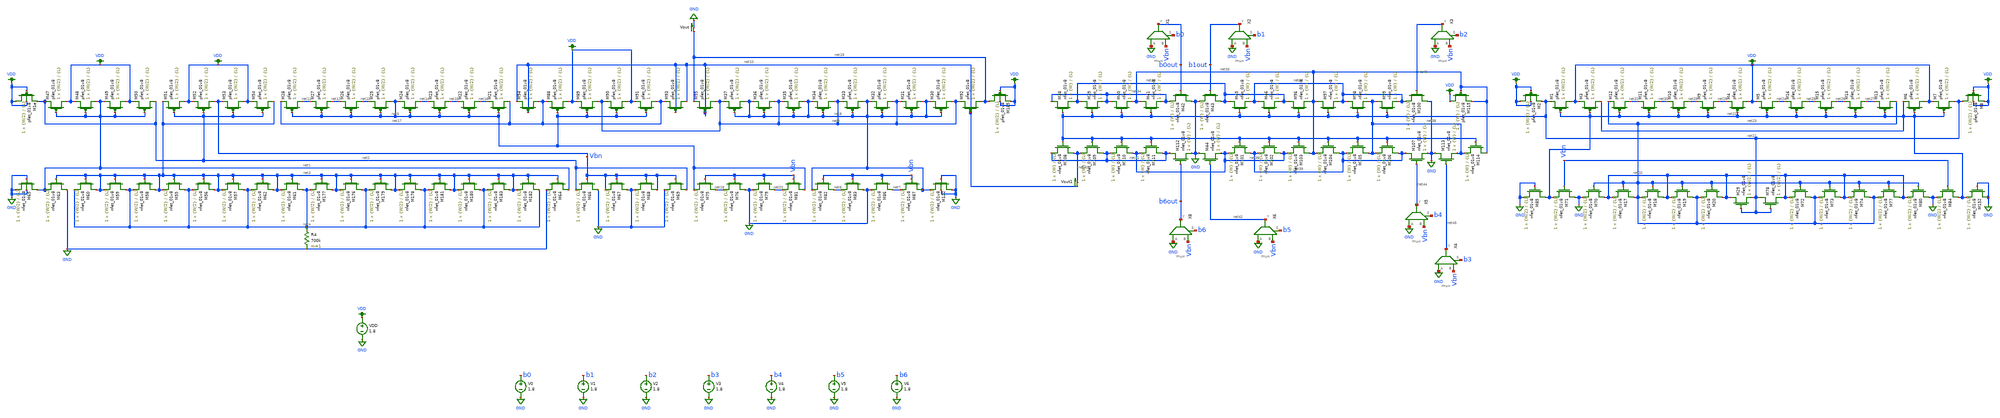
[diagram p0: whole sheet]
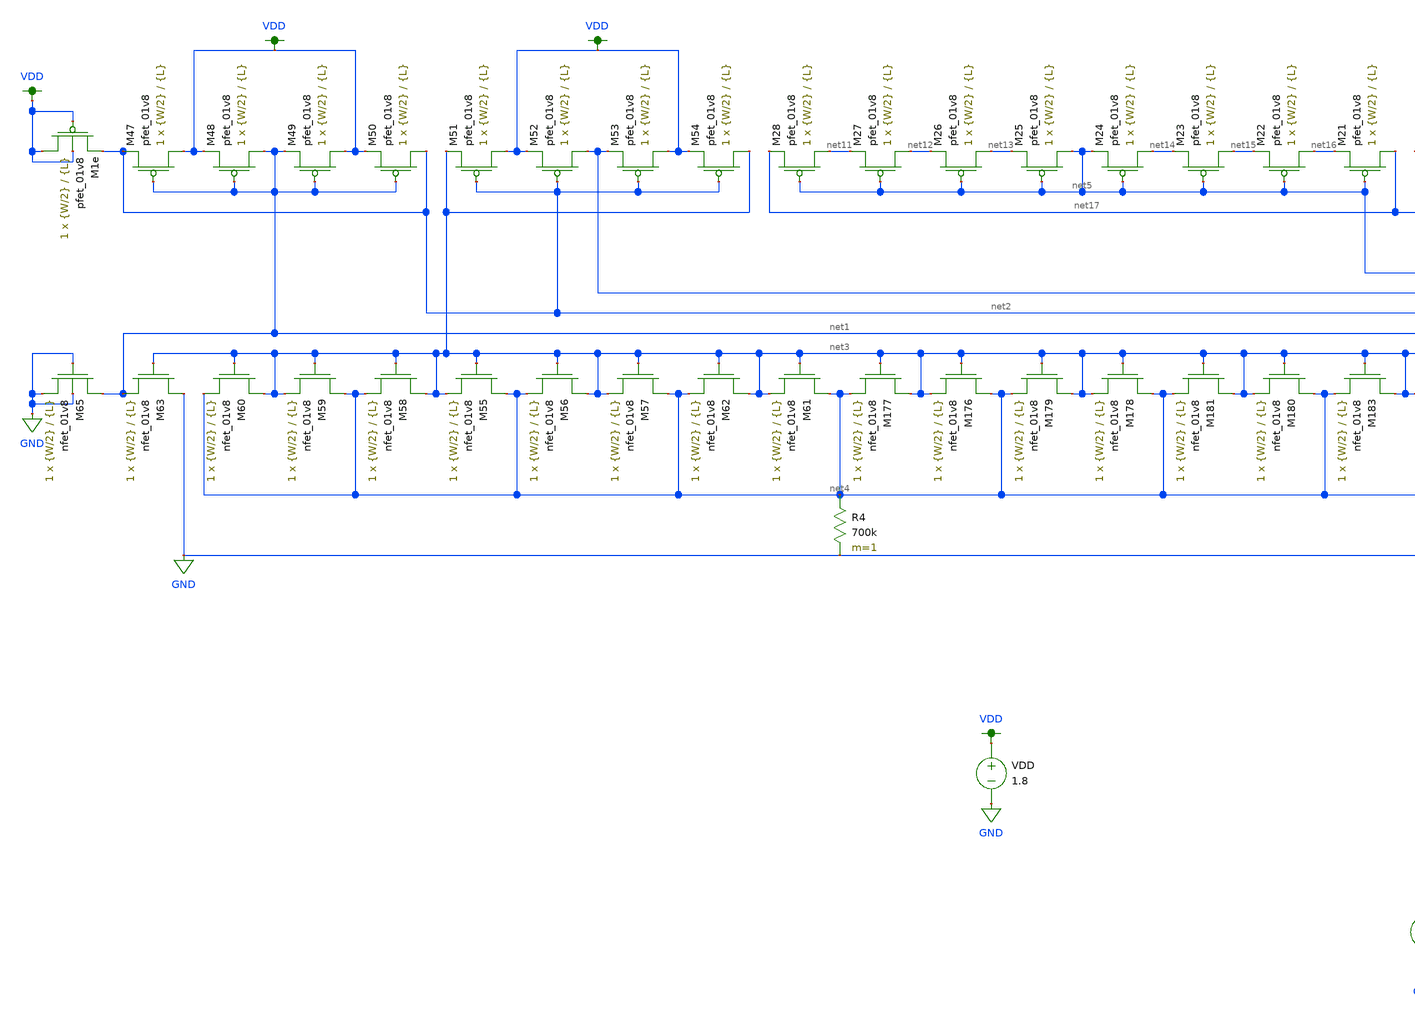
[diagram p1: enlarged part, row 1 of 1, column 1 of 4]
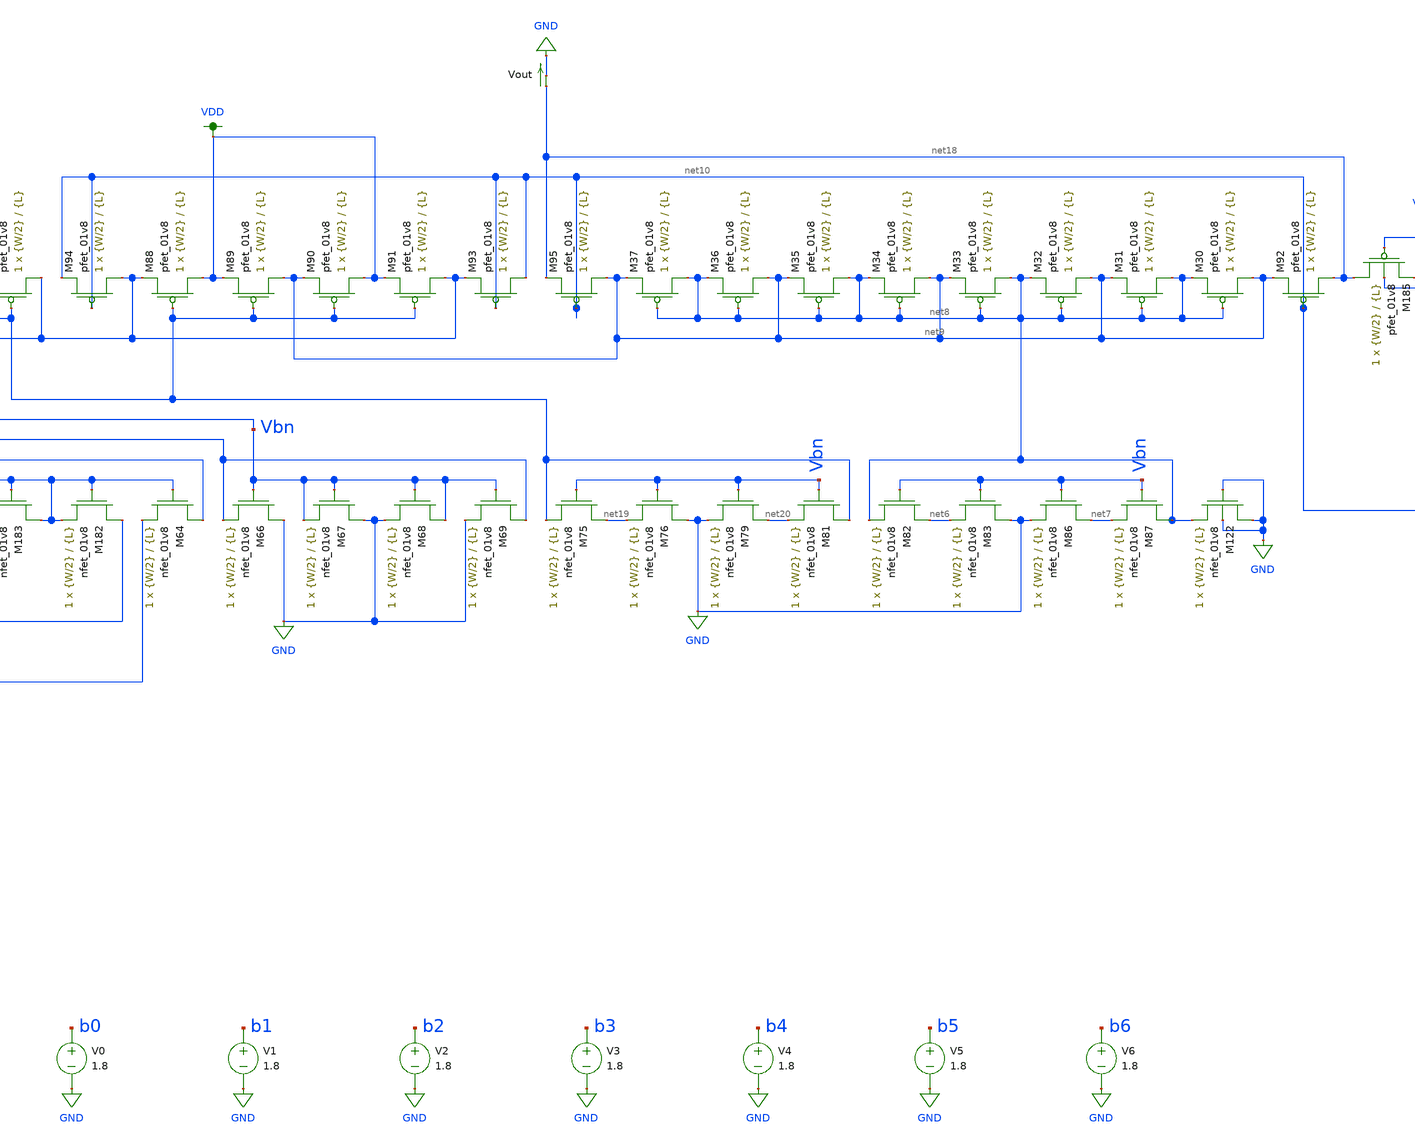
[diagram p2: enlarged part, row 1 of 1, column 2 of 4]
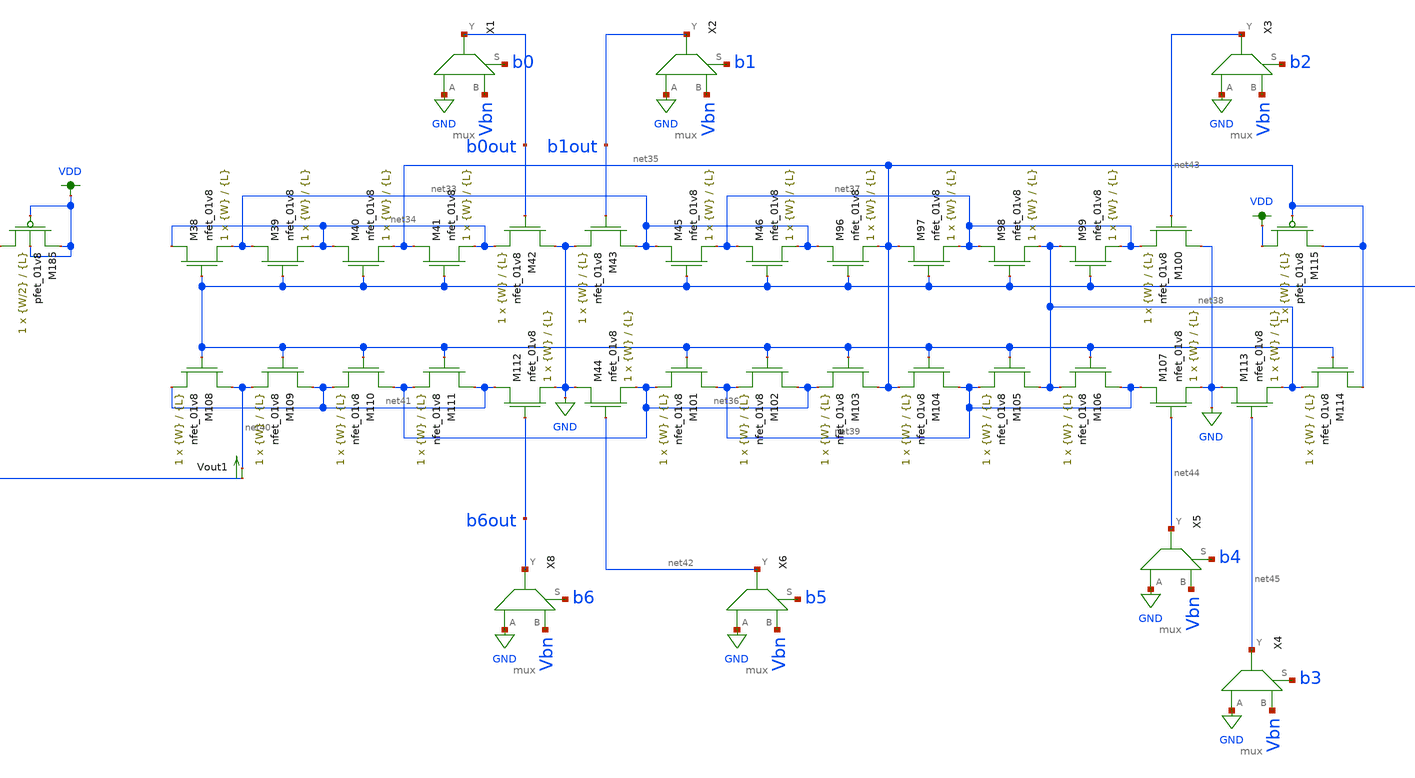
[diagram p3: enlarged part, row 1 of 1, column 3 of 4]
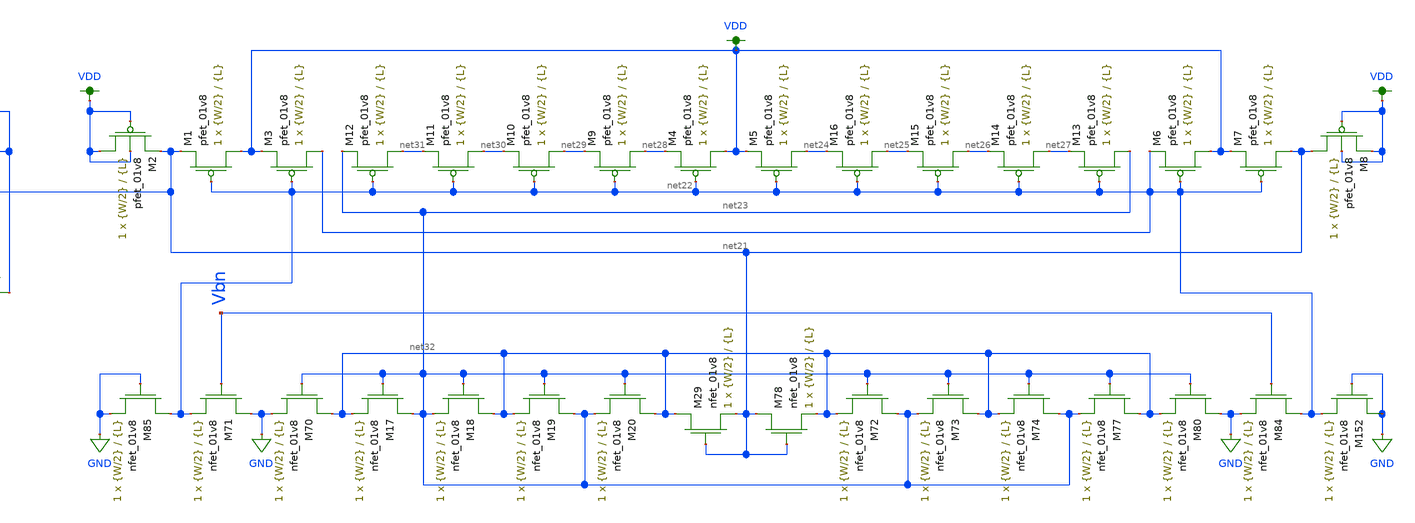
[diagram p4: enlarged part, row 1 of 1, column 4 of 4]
** sch_path: dac/schematics/misc/dac_dnl_inl_current_mirror_lds.sch
**.subckt dac_dnl_inl_current_mirror_lds
V0 b0 GND 1.8
V1 b1 GND 1.8
V2 b2 GND 1.8
V3 b3 GND 1.8
V4 b4 GND 1.8
V5 b5 GND 1.8
V6 b6 GND 1.8
VDD VDD GND 1.8
XM47 VDD net1 net2 VDD sky130_fd_pr__pfet_01v8 L={L} W={W/2} nf=1 ad='int((nf+1)/2) * W/nf * 0.29' as='int((nf+2)/2) * W/nf * 0.29'
+ pd='2*int((nf+1)/2) * (W/nf + 0.29)' ps='2*int((nf+2)/2) * (W/nf + 0.29)' nrd='0.29 / W' nrs='0.29 / W'
+ sa=0 sb=0 sd=0 mult=1 m=1
XM48 net1 net1 VDD VDD sky130_fd_pr__pfet_01v8 L={L} W={W/2} nf=1 ad='int((nf+1)/2) * W/nf * 0.29' as='int((nf+2)/2) * W/nf * 0.29'
+ pd='2*int((nf+1)/2) * (W/nf + 0.29)' ps='2*int((nf+2)/2) * (W/nf + 0.29)' nrd='0.29 / W' nrs='0.29 / W'
+ sa=0 sb=0 sd=0 mult=1 m=1
XM49 VDD net1 net1 VDD sky130_fd_pr__pfet_01v8 L={L} W={W/2} nf=1 ad='int((nf+1)/2) * W/nf * 0.29' as='int((nf+2)/2) * W/nf * 0.29'
+ pd='2*int((nf+1)/2) * (W/nf + 0.29)' ps='2*int((nf+2)/2) * (W/nf + 0.29)' nrd='0.29 / W' nrs='0.29 / W'
+ sa=0 sb=0 sd=0 mult=1 m=1
XM50 net2 net1 VDD VDD sky130_fd_pr__pfet_01v8 L={L} W={W/2} nf=1 ad='int((nf+1)/2) * W/nf * 0.29' as='int((nf+2)/2) * W/nf * 0.29'
+ pd='2*int((nf+1)/2) * (W/nf + 0.29)' ps='2*int((nf+2)/2) * (W/nf + 0.29)' nrd='0.29 / W' nrs='0.29 / W'
+ sa=0 sb=0 sd=0 mult=1 m=1
XM51 VDD net2 net3 VDD sky130_fd_pr__pfet_01v8 L={L} W={W/2} nf=1 ad='int((nf+1)/2) * W/nf * 0.29' as='int((nf+2)/2) * W/nf * 0.29'
+ pd='2*int((nf+1)/2) * (W/nf + 0.29)' ps='2*int((nf+2)/2) * (W/nf + 0.29)' nrd='0.29 / W' nrs='0.29 / W'
+ sa=0 sb=0 sd=0 mult=1 m=1
XM52 Vbn net2 VDD VDD sky130_fd_pr__pfet_01v8 L={L} W={W/2} nf=1 ad='int((nf+1)/2) * W/nf * 0.29' as='int((nf+2)/2) * W/nf * 0.29'
+ pd='2*int((nf+1)/2) * (W/nf + 0.29)' ps='2*int((nf+2)/2) * (W/nf + 0.29)' nrd='0.29 / W' nrs='0.29 / W'
+ sa=0 sb=0 sd=0 mult=1 m=1
XM53 VDD net2 Vbn VDD sky130_fd_pr__pfet_01v8 L={L} W={W/2} nf=1 ad='int((nf+1)/2) * W/nf * 0.29' as='int((nf+2)/2) * W/nf * 0.29'
+ pd='2*int((nf+1)/2) * (W/nf + 0.29)' ps='2*int((nf+2)/2) * (W/nf + 0.29)' nrd='0.29 / W' nrs='0.29 / W'
+ sa=0 sb=0 sd=0 mult=1 m=1
XM54 net3 net2 VDD VDD sky130_fd_pr__pfet_01v8 L={L} W={W/2} nf=1 ad='int((nf+1)/2) * W/nf * 0.29' as='int((nf+2)/2) * W/nf * 0.29'
+ pd='2*int((nf+1)/2) * (W/nf + 0.29)' ps='2*int((nf+2)/2) * (W/nf + 0.29)' nrd='0.29 / W' nrs='0.29 / W'
+ sa=0 sb=0 sd=0 mult=1 m=1
XM55 net4 net3 net3 GND sky130_fd_pr__nfet_01v8 L={L} W={W/2} nf=1 ad='int((nf+1)/2) * W/nf * 0.29' as='int((nf+2)/2) * W/nf * 0.29'
+ pd='2*int((nf+1)/2) * (W/nf + 0.29)' ps='2*int((nf+2)/2) * (W/nf + 0.29)' nrd='0.29 / W' nrs='0.29 / W'
+ sa=0 sb=0 sd=0 mult=1 m=1
XM56 net3 net3 net4 GND sky130_fd_pr__nfet_01v8 L={L} W={W/2} nf=1 ad='int((nf+1)/2) * W/nf * 0.29' as='int((nf+2)/2) * W/nf * 0.29'
+ pd='2*int((nf+1)/2) * (W/nf + 0.29)' ps='2*int((nf+2)/2) * (W/nf + 0.29)' nrd='0.29 / W' nrs='0.29 / W'
+ sa=0 sb=0 sd=0 mult=1 m=1
XM57 net4 net3 net3 GND sky130_fd_pr__nfet_01v8 L={L} W={W/2} nf=1 ad='int((nf+1)/2) * W/nf * 0.29' as='int((nf+2)/2) * W/nf * 0.29'
+ pd='2*int((nf+1)/2) * (W/nf + 0.29)' ps='2*int((nf+2)/2) * (W/nf + 0.29)' nrd='0.29 / W' nrs='0.29 / W'
+ sa=0 sb=0 sd=0 mult=1 m=1
XM58 net3 net3 net4 GND sky130_fd_pr__nfet_01v8 L={L} W={W/2} nf=1 ad='int((nf+1)/2) * W/nf * 0.29' as='int((nf+2)/2) * W/nf * 0.29'
+ pd='2*int((nf+1)/2) * (W/nf + 0.29)' ps='2*int((nf+2)/2) * (W/nf + 0.29)' nrd='0.29 / W' nrs='0.29 / W'
+ sa=0 sb=0 sd=0 mult=1 m=1
XM59 net4 net3 net3 GND sky130_fd_pr__nfet_01v8 L={L} W={W/2} nf=1 ad='int((nf+1)/2) * W/nf * 0.29' as='int((nf+2)/2) * W/nf * 0.29'
+ pd='2*int((nf+1)/2) * (W/nf + 0.29)' ps='2*int((nf+2)/2) * (W/nf + 0.29)' nrd='0.29 / W' nrs='0.29 / W'
+ sa=0 sb=0 sd=0 mult=1 m=1
XM60 net3 net3 net4 GND sky130_fd_pr__nfet_01v8 L={L} W={W/2} nf=1 ad='int((nf+1)/2) * W/nf * 0.29' as='int((nf+2)/2) * W/nf * 0.29'
+ pd='2*int((nf+1)/2) * (W/nf + 0.29)' ps='2*int((nf+2)/2) * (W/nf + 0.29)' nrd='0.29 / W' nrs='0.29 / W'
+ sa=0 sb=0 sd=0 mult=1 m=1
XM61 net4 net3 net3 GND sky130_fd_pr__nfet_01v8 L={L} W={W/2} nf=1 ad='int((nf+1)/2) * W/nf * 0.29' as='int((nf+2)/2) * W/nf * 0.29'
+ pd='2*int((nf+1)/2) * (W/nf + 0.29)' ps='2*int((nf+2)/2) * (W/nf + 0.29)' nrd='0.29 / W' nrs='0.29 / W'
+ sa=0 sb=0 sd=0 mult=1 m=1
XM62 net3 net3 net4 GND sky130_fd_pr__nfet_01v8 L={L} W={W/2} nf=1 ad='int((nf+1)/2) * W/nf * 0.29' as='int((nf+2)/2) * W/nf * 0.29'
+ pd='2*int((nf+1)/2) * (W/nf + 0.29)' ps='2*int((nf+2)/2) * (W/nf + 0.29)' nrd='0.29 / W' nrs='0.29 / W'
+ sa=0 sb=0 sd=0 mult=1 m=1
XM63 GND net3 net1 GND sky130_fd_pr__nfet_01v8 L={L} W={W/2} nf=1 ad='int((nf+1)/2) * W/nf * 0.29' as='int((nf+2)/2) * W/nf * 0.29'
+ pd='2*int((nf+1)/2) * (W/nf + 0.29)' ps='2*int((nf+2)/2) * (W/nf + 0.29)' nrd='0.29 / W' nrs='0.29 / W'
+ sa=0 sb=0 sd=0 mult=1 m=1
XM64 net1 net3 GND GND sky130_fd_pr__nfet_01v8 L={L} W={W/2} nf=1 ad='int((nf+1)/2) * W/nf * 0.29' as='int((nf+2)/2) * W/nf * 0.29'
+ pd='2*int((nf+1)/2) * (W/nf + 0.29)' ps='2*int((nf+2)/2) * (W/nf + 0.29)' nrd='0.29 / W' nrs='0.29 / W'
+ sa=0 sb=0 sd=0 mult=1 m=1
R4 net4 GND 700k m=1
XM1e VDD VDD net2 VDD sky130_fd_pr__pfet_01v8 L={L} W={W/2} nf=1 ad='int((nf+1)/2) * W/nf * 0.29' as='int((nf+2)/2) * W/nf * 0.29'
+ pd='2*int((nf+1)/2) * (W/nf + 0.29)' ps='2*int((nf+2)/2) * (W/nf + 0.29)' nrd='0.29 / W' nrs='0.29 / W'
+ sa=0 sb=0 sd=0 mult=1 m=1
XM65 net1 GND GND GND sky130_fd_pr__nfet_01v8 L={L} W={W/2} nf=1 ad='int((nf+1)/2) * W/nf * 0.29' as='int((nf+2)/2) * W/nf * 0.29'
+ pd='2*int((nf+1)/2) * (W/nf + 0.29)' ps='2*int((nf+2)/2) * (W/nf + 0.29)' nrd='0.29 / W' nrs='0.29 / W'
+ sa=0 sb=0 sd=0 mult=1 m=1
XM66 GND Vbn net2 GND sky130_fd_pr__nfet_01v8 L={L} W={W/2} nf=1 ad='int((nf+1)/2) * W/nf * 0.29' as='int((nf+2)/2) * W/nf * 0.29'
+ pd='2*int((nf+1)/2) * (W/nf + 0.29)' ps='2*int((nf+2)/2) * (W/nf + 0.29)' nrd='0.29 / W' nrs='0.29 / W'
+ sa=0 sb=0 sd=0 mult=1 m=1
XM67 GND Vbn Vbn GND sky130_fd_pr__nfet_01v8 L={L} W={W/2} nf=1 ad='int((nf+1)/2) * W/nf * 0.29' as='int((nf+2)/2) * W/nf * 0.29'
+ pd='2*int((nf+1)/2) * (W/nf + 0.29)' ps='2*int((nf+2)/2) * (W/nf + 0.29)' nrd='0.29 / W' nrs='0.29 / W'
+ sa=0 sb=0 sd=0 mult=1 m=1
XM68 Vbn Vbn GND GND sky130_fd_pr__nfet_01v8 L={L} W={W/2} nf=1 ad='int((nf+1)/2) * W/nf * 0.29' as='int((nf+2)/2) * W/nf * 0.29'
+ pd='2*int((nf+1)/2) * (W/nf + 0.29)' ps='2*int((nf+2)/2) * (W/nf + 0.29)' nrd='0.29 / W' nrs='0.29 / W'
+ sa=0 sb=0 sd=0 mult=1 m=1
XM69 net2 Vbn GND GND sky130_fd_pr__nfet_01v8 L={L} W={W/2} nf=1 ad='int((nf+1)/2) * W/nf * 0.29' as='int((nf+2)/2) * W/nf * 0.29'
+ pd='2*int((nf+1)/2) * (W/nf + 0.29)' ps='2*int((nf+2)/2) * (W/nf + 0.29)' nrd='0.29 / W' nrs='0.29 / W'
+ sa=0 sb=0 sd=0 mult=1 m=1
XM75 net19 Vbn net5 GND sky130_fd_pr__nfet_01v8 L={L} W={W/2} nf=1 ad='int((nf+1)/2) * W/nf * 0.29' as='int((nf+2)/2) * W/nf * 0.29'
+ pd='2*int((nf+1)/2) * (W/nf + 0.29)' ps='2*int((nf+2)/2) * (W/nf + 0.29)' nrd='0.29 / W' nrs='0.29 / W'
+ sa=0 sb=0 sd=0 mult=1 m=1
XM76 GND Vbn net19 GND sky130_fd_pr__nfet_01v8 L={L} W={W/2} nf=1 ad='int((nf+1)/2) * W/nf * 0.29' as='int((nf+2)/2) * W/nf * 0.29'
+ pd='2*int((nf+1)/2) * (W/nf + 0.29)' ps='2*int((nf+2)/2) * (W/nf + 0.29)' nrd='0.29 / W' nrs='0.29 / W'
+ sa=0 sb=0 sd=0 mult=1 m=1
XM79 net20 Vbn GND GND sky130_fd_pr__nfet_01v8 L={L} W={W/2} nf=1 ad='int((nf+1)/2) * W/nf * 0.29' as='int((nf+2)/2) * W/nf * 0.29'
+ pd='2*int((nf+1)/2) * (W/nf + 0.29)' ps='2*int((nf+2)/2) * (W/nf + 0.29)' nrd='0.29 / W' nrs='0.29 / W'
+ sa=0 sb=0 sd=0 mult=1 m=1
XM81 net5 Vbn net20 GND sky130_fd_pr__nfet_01v8 L={L} W={W/2} nf=1 ad='int((nf+1)/2) * W/nf * 0.29' as='int((nf+2)/2) * W/nf * 0.29'
+ pd='2*int((nf+1)/2) * (W/nf + 0.29)' ps='2*int((nf+2)/2) * (W/nf + 0.29)' nrd='0.29 / W' nrs='0.29 / W'
+ sa=0 sb=0 sd=0 mult=1 m=1
XM82 net6 Vbn net8 GND sky130_fd_pr__nfet_01v8 L={L} W={W/2} nf=1 ad='int((nf+1)/2) * W/nf * 0.29' as='int((nf+2)/2) * W/nf * 0.29'
+ pd='2*int((nf+1)/2) * (W/nf + 0.29)' ps='2*int((nf+2)/2) * (W/nf + 0.29)' nrd='0.29 / W' nrs='0.29 / W'
+ sa=0 sb=0 sd=0 mult=1 m=1
XM83 GND Vbn net6 GND sky130_fd_pr__nfet_01v8 L={L} W={W/2} nf=1 ad='int((nf+1)/2) * W/nf * 0.29' as='int((nf+2)/2) * W/nf * 0.29'
+ pd='2*int((nf+1)/2) * (W/nf + 0.29)' ps='2*int((nf+2)/2) * (W/nf + 0.29)' nrd='0.29 / W' nrs='0.29 / W'
+ sa=0 sb=0 sd=0 mult=1 m=1
XM86 net7 Vbn GND GND sky130_fd_pr__nfet_01v8 L={L} W={W/2} nf=1 ad='int((nf+1)/2) * W/nf * 0.29' as='int((nf+2)/2) * W/nf * 0.29'
+ pd='2*int((nf+1)/2) * (W/nf + 0.29)' ps='2*int((nf+2)/2) * (W/nf + 0.29)' nrd='0.29 / W' nrs='0.29 / W'
+ sa=0 sb=0 sd=0 mult=1 m=1
XM87 net8 Vbn net7 GND sky130_fd_pr__nfet_01v8 L={L} W={W/2} nf=1 ad='int((nf+1)/2) * W/nf * 0.29' as='int((nf+2)/2) * W/nf * 0.29'
+ pd='2*int((nf+1)/2) * (W/nf + 0.29)' ps='2*int((nf+2)/2) * (W/nf + 0.29)' nrd='0.29 / W' nrs='0.29 / W'
+ sa=0 sb=0 sd=0 mult=1 m=1
XM88 VDD net5 net17 VDD sky130_fd_pr__pfet_01v8 L={L} W={W/2} nf=1 ad='int((nf+1)/2) * W/nf * 0.29' as='int((nf+2)/2) * W/nf * 0.29'
+ pd='2*int((nf+1)/2) * (W/nf + 0.29)' ps='2*int((nf+2)/2) * (W/nf + 0.29)' nrd='0.29 / W' nrs='0.29 / W'
+ sa=0 sb=0 sd=0 mult=1 m=1
XM89 net9 net5 VDD VDD sky130_fd_pr__pfet_01v8 L={L} W={W/2} nf=1 ad='int((nf+1)/2) * W/nf * 0.29' as='int((nf+2)/2) * W/nf * 0.29'
+ pd='2*int((nf+1)/2) * (W/nf + 0.29)' ps='2*int((nf+2)/2) * (W/nf + 0.29)' nrd='0.29 / W' nrs='0.29 / W'
+ sa=0 sb=0 sd=0 mult=1 m=1
XM90 VDD net5 net9 VDD sky130_fd_pr__pfet_01v8 L={L} W={W/2} nf=1 ad='int((nf+1)/2) * W/nf * 0.29' as='int((nf+2)/2) * W/nf * 0.29'
+ pd='2*int((nf+1)/2) * (W/nf + 0.29)' ps='2*int((nf+2)/2) * (W/nf + 0.29)' nrd='0.29 / W' nrs='0.29 / W'
+ sa=0 sb=0 sd=0 mult=1 m=1
XM91 net17 net5 VDD VDD sky130_fd_pr__pfet_01v8 L={L} W={W/2} nf=1 ad='int((nf+1)/2) * W/nf * 0.29' as='int((nf+2)/2) * W/nf * 0.29'
+ pd='2*int((nf+1)/2) * (W/nf + 0.29)' ps='2*int((nf+2)/2) * (W/nf + 0.29)' nrd='0.29 / W' nrs='0.29 / W'
+ sa=0 sb=0 sd=0 mult=1 m=1
XM92 net18 net10 net9 VDD sky130_fd_pr__pfet_01v8 L={L} W={W/2} nf=1 ad='int((nf+1)/2) * W/nf * 0.29'
+ as='int((nf+2)/2) * W/nf * 0.29' pd='2*int((nf+1)/2) * (W/nf + 0.29)' ps='2*int((nf+2)/2) * (W/nf + 0.29)'
+ nrd='0.29 / W' nrs='0.29 / W' sa=0 sb=0 sd=0 mult=1 m=1
XM93 net10 net10 net17 VDD sky130_fd_pr__pfet_01v8 L={L} W={W/2} nf=1 ad='int((nf+1)/2) * W/nf * 0.29'
+ as='int((nf+2)/2) * W/nf * 0.29' pd='2*int((nf+1)/2) * (W/nf + 0.29)' ps='2*int((nf+2)/2) * (W/nf + 0.29)'
+ nrd='0.29 / W' nrs='0.29 / W' sa=0 sb=0 sd=0 mult=1 m=1
XM94 net17 net10 net10 VDD sky130_fd_pr__pfet_01v8 L={L} W={W/2} nf=1 ad='int((nf+1)/2) * W/nf * 0.29'
+ as='int((nf+2)/2) * W/nf * 0.29' pd='2*int((nf+1)/2) * (W/nf + 0.29)' ps='2*int((nf+2)/2) * (W/nf + 0.29)'
+ nrd='0.29 / W' nrs='0.29 / W' sa=0 sb=0 sd=0 mult=1 m=1
XM95 net9 net10 net18 VDD sky130_fd_pr__pfet_01v8 L={L} W={W/2} nf=1 ad='int((nf+1)/2) * W/nf * 0.29'
+ as='int((nf+2)/2) * W/nf * 0.29' pd='2*int((nf+1)/2) * (W/nf + 0.29)' ps='2*int((nf+2)/2) * (W/nf + 0.29)'
+ nrd='0.29 / W' nrs='0.29 / W' sa=0 sb=0 sd=0 mult=1 m=1
XM176 net4 net3 net3 GND sky130_fd_pr__nfet_01v8 L={L} W={W/2} nf=1 ad='int((nf+1)/2) * W/nf * 0.29'
+ as='int((nf+2)/2) * W/nf * 0.29' pd='2*int((nf+1)/2) * (W/nf + 0.29)' ps='2*int((nf+2)/2) * (W/nf + 0.29)'
+ nrd='0.29 / W' nrs='0.29 / W' sa=0 sb=0 sd=0 mult=1 m=1
XM177 net3 net3 net4 GND sky130_fd_pr__nfet_01v8 L={L} W={W/2} nf=1 ad='int((nf+1)/2) * W/nf * 0.29'
+ as='int((nf+2)/2) * W/nf * 0.29' pd='2*int((nf+1)/2) * (W/nf + 0.29)' ps='2*int((nf+2)/2) * (W/nf + 0.29)'
+ nrd='0.29 / W' nrs='0.29 / W' sa=0 sb=0 sd=0 mult=1 m=1
XM178 net4 net3 net3 GND sky130_fd_pr__nfet_01v8 L={L} W={W/2} nf=1 ad='int((nf+1)/2) * W/nf * 0.29'
+ as='int((nf+2)/2) * W/nf * 0.29' pd='2*int((nf+1)/2) * (W/nf + 0.29)' ps='2*int((nf+2)/2) * (W/nf + 0.29)'
+ nrd='0.29 / W' nrs='0.29 / W' sa=0 sb=0 sd=0 mult=1 m=1
XM179 net3 net3 net4 GND sky130_fd_pr__nfet_01v8 L={L} W={W/2} nf=1 ad='int((nf+1)/2) * W/nf * 0.29'
+ as='int((nf+2)/2) * W/nf * 0.29' pd='2*int((nf+1)/2) * (W/nf + 0.29)' ps='2*int((nf+2)/2) * (W/nf + 0.29)'
+ nrd='0.29 / W' nrs='0.29 / W' sa=0 sb=0 sd=0 mult=1 m=1
XM180 net4 net3 net3 GND sky130_fd_pr__nfet_01v8 L={L} W={W/2} nf=1 ad='int((nf+1)/2) * W/nf * 0.29'
+ as='int((nf+2)/2) * W/nf * 0.29' pd='2*int((nf+1)/2) * (W/nf + 0.29)' ps='2*int((nf+2)/2) * (W/nf + 0.29)'
+ nrd='0.29 / W' nrs='0.29 / W' sa=0 sb=0 sd=0 mult=1 m=1
XM181 net3 net3 net4 GND sky130_fd_pr__nfet_01v8 L={L} W={W/2} nf=1 ad='int((nf+1)/2) * W/nf * 0.29'
+ as='int((nf+2)/2) * W/nf * 0.29' pd='2*int((nf+1)/2) * (W/nf + 0.29)' ps='2*int((nf+2)/2) * (W/nf + 0.29)'
+ nrd='0.29 / W' nrs='0.29 / W' sa=0 sb=0 sd=0 mult=1 m=1
XM182 net4 net3 net3 GND sky130_fd_pr__nfet_01v8 L={L} W={W/2} nf=1 ad='int((nf+1)/2) * W/nf * 0.29'
+ as='int((nf+2)/2) * W/nf * 0.29' pd='2*int((nf+1)/2) * (W/nf + 0.29)' ps='2*int((nf+2)/2) * (W/nf + 0.29)'
+ nrd='0.29 / W' nrs='0.29 / W' sa=0 sb=0 sd=0 mult=1 m=1
XM183 net3 net3 net4 GND sky130_fd_pr__nfet_01v8 L={L} W={W/2} nf=1 ad='int((nf+1)/2) * W/nf * 0.29'
+ as='int((nf+2)/2) * W/nf * 0.29' pd='2*int((nf+1)/2) * (W/nf + 0.29)' ps='2*int((nf+2)/2) * (W/nf + 0.29)'
+ nrd='0.29 / W' nrs='0.29 / W' sa=0 sb=0 sd=0 mult=1 m=1
XM185 net18 VDD VDD VDD sky130_fd_pr__pfet_01v8 L={L} W={W/2} nf=1 ad='int((nf+1)/2) * W/nf * 0.29' as='int((nf+2)/2) * W/nf * 0.29'
+ pd='2*int((nf+1)/2) * (W/nf + 0.29)' ps='2*int((nf+2)/2) * (W/nf + 0.29)' nrd='0.29 / W' nrs='0.29 / W'
+ sa=0 sb=0 sd=0 mult=1 m=1
Vout net18 GND 0
.save i(vout)
XM21 net17 net5 net16 VDD sky130_fd_pr__pfet_01v8 L={L} W={W/2} nf=1 ad='int((nf+1)/2) * W/nf * 0.29'
+ as='int((nf+2)/2) * W/nf * 0.29' pd='2*int((nf+1)/2) * (W/nf + 0.29)' ps='2*int((nf+2)/2) * (W/nf + 0.29)'
+ nrd='0.29 / W' nrs='0.29 / W' sa=0 sb=0 sd=0 mult=1 m=1
XM22 net16 net5 net15 VDD sky130_fd_pr__pfet_01v8 L={L} W={W/2} nf=1 ad='int((nf+1)/2) * W/nf * 0.29'
+ as='int((nf+2)/2) * W/nf * 0.29' pd='2*int((nf+1)/2) * (W/nf + 0.29)' ps='2*int((nf+2)/2) * (W/nf + 0.29)'
+ nrd='0.29 / W' nrs='0.29 / W' sa=0 sb=0 sd=0 mult=1 m=1
XM23 net15 net5 net14 VDD sky130_fd_pr__pfet_01v8 L={L} W={W/2} nf=1 ad='int((nf+1)/2) * W/nf * 0.29'
+ as='int((nf+2)/2) * W/nf * 0.29' pd='2*int((nf+1)/2) * (W/nf + 0.29)' ps='2*int((nf+2)/2) * (W/nf + 0.29)'
+ nrd='0.29 / W' nrs='0.29 / W' sa=0 sb=0 sd=0 mult=1 m=1
XM24 net14 net5 net5 VDD sky130_fd_pr__pfet_01v8 L={L} W={W/2} nf=1 ad='int((nf+1)/2) * W/nf * 0.29'
+ as='int((nf+2)/2) * W/nf * 0.29' pd='2*int((nf+1)/2) * (W/nf + 0.29)' ps='2*int((nf+2)/2) * (W/nf + 0.29)'
+ nrd='0.29 / W' nrs='0.29 / W' sa=0 sb=0 sd=0 mult=1 m=1
XM25 net5 net5 net13 VDD sky130_fd_pr__pfet_01v8 L={L} W={W/2} nf=1 ad='int((nf+1)/2) * W/nf * 0.29'
+ as='int((nf+2)/2) * W/nf * 0.29' pd='2*int((nf+1)/2) * (W/nf + 0.29)' ps='2*int((nf+2)/2) * (W/nf + 0.29)'
+ nrd='0.29 / W' nrs='0.29 / W' sa=0 sb=0 sd=0 mult=1 m=1
XM26 net13 net5 net12 VDD sky130_fd_pr__pfet_01v8 L={L} W={W/2} nf=1 ad='int((nf+1)/2) * W/nf * 0.29'
+ as='int((nf+2)/2) * W/nf * 0.29' pd='2*int((nf+1)/2) * (W/nf + 0.29)' ps='2*int((nf+2)/2) * (W/nf + 0.29)'
+ nrd='0.29 / W' nrs='0.29 / W' sa=0 sb=0 sd=0 mult=1 m=1
XM27 net12 net5 net11 VDD sky130_fd_pr__pfet_01v8 L={L} W={W/2} nf=1 ad='int((nf+1)/2) * W/nf * 0.29'
+ as='int((nf+2)/2) * W/nf * 0.29' pd='2*int((nf+1)/2) * (W/nf + 0.29)' ps='2*int((nf+2)/2) * (W/nf + 0.29)'
+ nrd='0.29 / W' nrs='0.29 / W' sa=0 sb=0 sd=0 mult=1 m=1
XM28 net11 net5 net17 VDD sky130_fd_pr__pfet_01v8 L={L} W={W/2} nf=1 ad='int((nf+1)/2) * W/nf * 0.29'
+ as='int((nf+2)/2) * W/nf * 0.29' pd='2*int((nf+1)/2) * (W/nf + 0.29)' ps='2*int((nf+2)/2) * (W/nf + 0.29)'
+ nrd='0.29 / W' nrs='0.29 / W' sa=0 sb=0 sd=0 mult=1 m=1
XM30 net9 net8 net8 VDD sky130_fd_pr__pfet_01v8 L={L} W={W/2} nf=1 ad='int((nf+1)/2) * W/nf * 0.29' as='int((nf+2)/2) * W/nf * 0.29'
+ pd='2*int((nf+1)/2) * (W/nf + 0.29)' ps='2*int((nf+2)/2) * (W/nf + 0.29)' nrd='0.29 / W' nrs='0.29 / W'
+ sa=0 sb=0 sd=0 mult=1 m=1
XM31 net8 net8 net9 VDD sky130_fd_pr__pfet_01v8 L={L} W={W/2} nf=1 ad='int((nf+1)/2) * W/nf * 0.29' as='int((nf+2)/2) * W/nf * 0.29'
+ pd='2*int((nf+1)/2) * (W/nf + 0.29)' ps='2*int((nf+2)/2) * (W/nf + 0.29)' nrd='0.29 / W' nrs='0.29 / W'
+ sa=0 sb=0 sd=0 mult=1 m=1
XM32 net9 net8 net8 VDD sky130_fd_pr__pfet_01v8 L={L} W={W/2} nf=1 ad='int((nf+1)/2) * W/nf * 0.29' as='int((nf+2)/2) * W/nf * 0.29'
+ pd='2*int((nf+1)/2) * (W/nf + 0.29)' ps='2*int((nf+2)/2) * (W/nf + 0.29)' nrd='0.29 / W' nrs='0.29 / W'
+ sa=0 sb=0 sd=0 mult=1 m=1
XM33 net8 net8 net9 VDD sky130_fd_pr__pfet_01v8 L={L} W={W/2} nf=1 ad='int((nf+1)/2) * W/nf * 0.29' as='int((nf+2)/2) * W/nf * 0.29'
+ pd='2*int((nf+1)/2) * (W/nf + 0.29)' ps='2*int((nf+2)/2) * (W/nf + 0.29)' nrd='0.29 / W' nrs='0.29 / W'
+ sa=0 sb=0 sd=0 mult=1 m=1
XM34 net9 net8 net8 VDD sky130_fd_pr__pfet_01v8 L={L} W={W/2} nf=1 ad='int((nf+1)/2) * W/nf * 0.29' as='int((nf+2)/2) * W/nf * 0.29'
+ pd='2*int((nf+1)/2) * (W/nf + 0.29)' ps='2*int((nf+2)/2) * (W/nf + 0.29)' nrd='0.29 / W' nrs='0.29 / W'
+ sa=0 sb=0 sd=0 mult=1 m=1
XM35 net8 net8 net9 VDD sky130_fd_pr__pfet_01v8 L={L} W={W/2} nf=1 ad='int((nf+1)/2) * W/nf * 0.29' as='int((nf+2)/2) * W/nf * 0.29'
+ pd='2*int((nf+1)/2) * (W/nf + 0.29)' ps='2*int((nf+2)/2) * (W/nf + 0.29)' nrd='0.29 / W' nrs='0.29 / W'
+ sa=0 sb=0 sd=0 mult=1 m=1
XM36 net9 net8 net8 VDD sky130_fd_pr__pfet_01v8 L={L} W={W/2} nf=1 ad='int((nf+1)/2) * W/nf * 0.29' as='int((nf+2)/2) * W/nf * 0.29'
+ pd='2*int((nf+1)/2) * (W/nf + 0.29)' ps='2*int((nf+2)/2) * (W/nf + 0.29)' nrd='0.29 / W' nrs='0.29 / W'
+ sa=0 sb=0 sd=0 mult=1 m=1
XM37 net8 net8 net9 VDD sky130_fd_pr__pfet_01v8 L={L} W={W/2} nf=1 ad='int((nf+1)/2) * W/nf * 0.29' as='int((nf+2)/2) * W/nf * 0.29'
+ pd='2*int((nf+1)/2) * (W/nf + 0.29)' ps='2*int((nf+2)/2) * (W/nf + 0.29)' nrd='0.29 / W' nrs='0.29 / W'
+ sa=0 sb=0 sd=0 mult=1 m=1
XM122 GND GND net8 GND sky130_fd_pr__nfet_01v8 L={L} W={W/2} nf=1 ad='int((nf+1)/2) * W/nf * 0.29' as='int((nf+2)/2) * W/nf * 0.29'
+ pd='2*int((nf+1)/2) * (W/nf + 0.29)' ps='2*int((nf+2)/2) * (W/nf + 0.29)' nrd='0.29 / W' nrs='0.29 / W'
+ sa=0 sb=0 sd=0 mult=1 m=1
XM1 VDD net22 net21 VDD sky130_fd_pr__pfet_01v8 L={L} W={W/2} nf=1 ad='int((nf+1)/2) * W/nf * 0.29' as='int((nf+2)/2) * W/nf * 0.29'
+ pd='2*int((nf+1)/2) * (W/nf + 0.29)' ps='2*int((nf+2)/2) * (W/nf + 0.29)' nrd='0.29 / W' nrs='0.29 / W'
+ sa=0 sb=0 sd=0 mult=1 m=1
XM2 VDD VDD net21 VDD sky130_fd_pr__pfet_01v8 L={L} W={W/2} nf=1 ad='int((nf+1)/2) * W/nf * 0.29' as='int((nf+2)/2) * W/nf * 0.29'
+ pd='2*int((nf+1)/2) * (W/nf + 0.29)' ps='2*int((nf+2)/2) * (W/nf + 0.29)' nrd='0.29 / W' nrs='0.29 / W'
+ sa=0 sb=0 sd=0 mult=1 m=1
XM3 net22 net22 VDD VDD sky130_fd_pr__pfet_01v8 L={L} W={W/2} nf=1 ad='int((nf+1)/2) * W/nf * 0.29' as='int((nf+2)/2) * W/nf * 0.29'
+ pd='2*int((nf+1)/2) * (W/nf + 0.29)' ps='2*int((nf+2)/2) * (W/nf + 0.29)' nrd='0.29 / W' nrs='0.29 / W'
+ sa=0 sb=0 sd=0 mult=1 m=1
XM4 VDD net22 net28 VDD sky130_fd_pr__pfet_01v8 L={L} W={W/2} nf=1 ad='int((nf+1)/2) * W/nf * 0.29' as='int((nf+2)/2) * W/nf * 0.29'
+ pd='2*int((nf+1)/2) * (W/nf + 0.29)' ps='2*int((nf+2)/2) * (W/nf + 0.29)' nrd='0.29 / W' nrs='0.29 / W'
+ sa=0 sb=0 sd=0 mult=1 m=1
XM5 net24 net22 VDD VDD sky130_fd_pr__pfet_01v8 L={L} W={W/2} nf=1 ad='int((nf+1)/2) * W/nf * 0.29' as='int((nf+2)/2) * W/nf * 0.29'
+ pd='2*int((nf+1)/2) * (W/nf + 0.29)' ps='2*int((nf+2)/2) * (W/nf + 0.29)' nrd='0.29 / W' nrs='0.29 / W'
+ sa=0 sb=0 sd=0 mult=1 m=1
XM6 VDD net22 net22 VDD sky130_fd_pr__pfet_01v8 L={L} W={W/2} nf=1 ad='int((nf+1)/2) * W/nf * 0.29' as='int((nf+2)/2) * W/nf * 0.29'
+ pd='2*int((nf+1)/2) * (W/nf + 0.29)' ps='2*int((nf+2)/2) * (W/nf + 0.29)' nrd='0.29 / W' nrs='0.29 / W'
+ sa=0 sb=0 sd=0 mult=1 m=1
XM7 net21 net22 VDD VDD sky130_fd_pr__pfet_01v8 L={L} W={W/2} nf=1 ad='int((nf+1)/2) * W/nf * 0.29' as='int((nf+2)/2) * W/nf * 0.29'
+ pd='2*int((nf+1)/2) * (W/nf + 0.29)' ps='2*int((nf+2)/2) * (W/nf + 0.29)' nrd='0.29 / W' nrs='0.29 / W'
+ sa=0 sb=0 sd=0 mult=1 m=1
XM8 net21 VDD VDD VDD sky130_fd_pr__pfet_01v8 L={L} W={W/2} nf=1 ad='int((nf+1)/2) * W/nf * 0.29' as='int((nf+2)/2) * W/nf * 0.29'
+ pd='2*int((nf+1)/2) * (W/nf + 0.29)' ps='2*int((nf+2)/2) * (W/nf + 0.29)' nrd='0.29 / W' nrs='0.29 / W'
+ sa=0 sb=0 sd=0 mult=1 m=1
XM9 net28 net22 net29 VDD sky130_fd_pr__pfet_01v8 L={L} W={W/2} nf=1 ad='int((nf+1)/2) * W/nf * 0.29'
+ as='int((nf+2)/2) * W/nf * 0.29' pd='2*int((nf+1)/2) * (W/nf + 0.29)' ps='2*int((nf+2)/2) * (W/nf + 0.29)'
+ nrd='0.29 / W' nrs='0.29 / W' sa=0 sb=0 sd=0 mult=1 m=1
XM10 net29 net22 net30 VDD sky130_fd_pr__pfet_01v8 L={L} W={W/2} nf=1 ad='int((nf+1)/2) * W/nf * 0.29'
+ as='int((nf+2)/2) * W/nf * 0.29' pd='2*int((nf+1)/2) * (W/nf + 0.29)' ps='2*int((nf+2)/2) * (W/nf + 0.29)'
+ nrd='0.29 / W' nrs='0.29 / W' sa=0 sb=0 sd=0 mult=1 m=1
XM11 net30 net22 net31 VDD sky130_fd_pr__pfet_01v8 L={L} W={W/2} nf=1 ad='int((nf+1)/2) * W/nf * 0.29'
+ as='int((nf+2)/2) * W/nf * 0.29' pd='2*int((nf+1)/2) * (W/nf + 0.29)' ps='2*int((nf+2)/2) * (W/nf + 0.29)'
+ nrd='0.29 / W' nrs='0.29 / W' sa=0 sb=0 sd=0 mult=1 m=1
XM12 net31 net22 net23 VDD sky130_fd_pr__pfet_01v8 L={L} W={W/2} nf=1 ad='int((nf+1)/2) * W/nf * 0.29'
+ as='int((nf+2)/2) * W/nf * 0.29' pd='2*int((nf+1)/2) * (W/nf + 0.29)' ps='2*int((nf+2)/2) * (W/nf + 0.29)'
+ nrd='0.29 / W' nrs='0.29 / W' sa=0 sb=0 sd=0 mult=1 m=1
XM13 net23 net22 net27 VDD sky130_fd_pr__pfet_01v8 L={L} W={W/2} nf=1 ad='int((nf+1)/2) * W/nf * 0.29'
+ as='int((nf+2)/2) * W/nf * 0.29' pd='2*int((nf+1)/2) * (W/nf + 0.29)' ps='2*int((nf+2)/2) * (W/nf + 0.29)'
+ nrd='0.29 / W' nrs='0.29 / W' sa=0 sb=0 sd=0 mult=1 m=1
XM14 net27 net22 net26 VDD sky130_fd_pr__pfet_01v8 L={L} W={W/2} nf=1 ad='int((nf+1)/2) * W/nf * 0.29'
+ as='int((nf+2)/2) * W/nf * 0.29' pd='2*int((nf+1)/2) * (W/nf + 0.29)' ps='2*int((nf+2)/2) * (W/nf + 0.29)'
+ nrd='0.29 / W' nrs='0.29 / W' sa=0 sb=0 sd=0 mult=1 m=1
XM15 net26 net22 net25 VDD sky130_fd_pr__pfet_01v8 L={L} W={W/2} nf=1 ad='int((nf+1)/2) * W/nf * 0.29'
+ as='int((nf+2)/2) * W/nf * 0.29' pd='2*int((nf+1)/2) * (W/nf + 0.29)' ps='2*int((nf+2)/2) * (W/nf + 0.29)'
+ nrd='0.29 / W' nrs='0.29 / W' sa=0 sb=0 sd=0 mult=1 m=1
XM16 net25 net22 net24 VDD sky130_fd_pr__pfet_01v8 L={L} W={W/2} nf=1 ad='int((nf+1)/2) * W/nf * 0.29'
+ as='int((nf+2)/2) * W/nf * 0.29' pd='2*int((nf+1)/2) * (W/nf + 0.29)' ps='2*int((nf+2)/2) * (W/nf + 0.29)'
+ nrd='0.29 / W' nrs='0.29 / W' sa=0 sb=0 sd=0 mult=1 m=1
XM17 net23 net23 net32 GND sky130_fd_pr__nfet_01v8 L={L} W={W/2} nf=1 ad='int((nf+1)/2) * W/nf * 0.29'
+ as='int((nf+2)/2) * W/nf * 0.29' pd='2*int((nf+1)/2) * (W/nf + 0.29)' ps='2*int((nf+2)/2) * (W/nf + 0.29)'
+ nrd='0.29 / W' nrs='0.29 / W' sa=0 sb=0 sd=0 mult=1 m=1
XM18 net32 net23 net23 GND sky130_fd_pr__nfet_01v8 L={L} W={W/2} nf=1 ad='int((nf+1)/2) * W/nf * 0.29'
+ as='int((nf+2)/2) * W/nf * 0.29' pd='2*int((nf+1)/2) * (W/nf + 0.29)' ps='2*int((nf+2)/2) * (W/nf + 0.29)'
+ nrd='0.29 / W' nrs='0.29 / W' sa=0 sb=0 sd=0 mult=1 m=1
XM19 net23 net23 net32 GND sky130_fd_pr__nfet_01v8 L={L} W={W/2} nf=1 ad='int((nf+1)/2) * W/nf * 0.29'
+ as='int((nf+2)/2) * W/nf * 0.29' pd='2*int((nf+1)/2) * (W/nf + 0.29)' ps='2*int((nf+2)/2) * (W/nf + 0.29)'
+ nrd='0.29 / W' nrs='0.29 / W' sa=0 sb=0 sd=0 mult=1 m=1
XM20 net32 net23 net23 GND sky130_fd_pr__nfet_01v8 L={L} W={W/2} nf=1 ad='int((nf+1)/2) * W/nf * 0.29'
+ as='int((nf+2)/2) * W/nf * 0.29' pd='2*int((nf+1)/2) * (W/nf + 0.29)' ps='2*int((nf+2)/2) * (W/nf + 0.29)'
+ nrd='0.29 / W' nrs='0.29 / W' sa=0 sb=0 sd=0 mult=1 m=1
XM29 net32 net21 net21 GND sky130_fd_pr__nfet_01v8 L={L} W={W/2} nf=1 ad='int((nf+1)/2) * W/nf * 0.29'
+ as='int((nf+2)/2) * W/nf * 0.29' pd='2*int((nf+1)/2) * (W/nf + 0.29)' ps='2*int((nf+2)/2) * (W/nf + 0.29)'
+ nrd='0.29 / W' nrs='0.29 / W' sa=0 sb=0 sd=0 mult=1 m=1
XM70 net32 net23 GND GND sky130_fd_pr__nfet_01v8 L={L} W={W/2} nf=1 ad='int((nf+1)/2) * W/nf * 0.29'
+ as='int((nf+2)/2) * W/nf * 0.29' pd='2*int((nf+1)/2) * (W/nf + 0.29)' ps='2*int((nf+2)/2) * (W/nf + 0.29)'
+ nrd='0.29 / W' nrs='0.29 / W' sa=0 sb=0 sd=0 mult=1 m=1
XM71 GND Vbn net22 GND sky130_fd_pr__nfet_01v8 L={L} W={W/2} nf=1 ad='int((nf+1)/2) * W/nf * 0.29' as='int((nf+2)/2) * W/nf * 0.29'
+ pd='2*int((nf+1)/2) * (W/nf + 0.29)' ps='2*int((nf+2)/2) * (W/nf + 0.29)' nrd='0.29 / W' nrs='0.29 / W'
+ sa=0 sb=0 sd=0 mult=1 m=1
XM72 net23 net23 net32 GND sky130_fd_pr__nfet_01v8 L={L} W={W/2} nf=1 ad='int((nf+1)/2) * W/nf * 0.29'
+ as='int((nf+2)/2) * W/nf * 0.29' pd='2*int((nf+1)/2) * (W/nf + 0.29)' ps='2*int((nf+2)/2) * (W/nf + 0.29)'
+ nrd='0.29 / W' nrs='0.29 / W' sa=0 sb=0 sd=0 mult=1 m=1
XM73 net32 net23 net23 GND sky130_fd_pr__nfet_01v8 L={L} W={W/2} nf=1 ad='int((nf+1)/2) * W/nf * 0.29'
+ as='int((nf+2)/2) * W/nf * 0.29' pd='2*int((nf+1)/2) * (W/nf + 0.29)' ps='2*int((nf+2)/2) * (W/nf + 0.29)'
+ nrd='0.29 / W' nrs='0.29 / W' sa=0 sb=0 sd=0 mult=1 m=1
XM74 net23 net23 net32 GND sky130_fd_pr__nfet_01v8 L={L} W={W/2} nf=1 ad='int((nf+1)/2) * W/nf * 0.29'
+ as='int((nf+2)/2) * W/nf * 0.29' pd='2*int((nf+1)/2) * (W/nf + 0.29)' ps='2*int((nf+2)/2) * (W/nf + 0.29)'
+ nrd='0.29 / W' nrs='0.29 / W' sa=0 sb=0 sd=0 mult=1 m=1
XM77 net32 net23 net23 GND sky130_fd_pr__nfet_01v8 L={L} W={W/2} nf=1 ad='int((nf+1)/2) * W/nf * 0.29'
+ as='int((nf+2)/2) * W/nf * 0.29' pd='2*int((nf+1)/2) * (W/nf + 0.29)' ps='2*int((nf+2)/2) * (W/nf + 0.29)'
+ nrd='0.29 / W' nrs='0.29 / W' sa=0 sb=0 sd=0 mult=1 m=1
XM78 net21 net21 net32 GND sky130_fd_pr__nfet_01v8 L={L} W={W/2} nf=1 ad='int((nf+1)/2) * W/nf * 0.29'
+ as='int((nf+2)/2) * W/nf * 0.29' pd='2*int((nf+1)/2) * (W/nf + 0.29)' ps='2*int((nf+2)/2) * (W/nf + 0.29)'
+ nrd='0.29 / W' nrs='0.29 / W' sa=0 sb=0 sd=0 mult=1 m=1
XM80 GND net23 net32 GND sky130_fd_pr__nfet_01v8 L={L} W={W/2} nf=1 ad='int((nf+1)/2) * W/nf * 0.29'
+ as='int((nf+2)/2) * W/nf * 0.29' pd='2*int((nf+1)/2) * (W/nf + 0.29)' ps='2*int((nf+2)/2) * (W/nf + 0.29)'
+ nrd='0.29 / W' nrs='0.29 / W' sa=0 sb=0 sd=0 mult=1 m=1
XM84 net22 Vbn GND GND sky130_fd_pr__nfet_01v8 L={L} W={W/2} nf=1 ad='int((nf+1)/2) * W/nf * 0.29' as='int((nf+2)/2) * W/nf * 0.29'
+ pd='2*int((nf+1)/2) * (W/nf + 0.29)' ps='2*int((nf+2)/2) * (W/nf + 0.29)' nrd='0.29 / W' nrs='0.29 / W'
+ sa=0 sb=0 sd=0 mult=1 m=1
XM85 net22 GND GND GND sky130_fd_pr__nfet_01v8 L={L} W={W/2} nf=1 ad='int((nf+1)/2) * W/nf * 0.29' as='int((nf+2)/2) * W/nf * 0.29'
+ pd='2*int((nf+1)/2) * (W/nf + 0.29)' ps='2*int((nf+2)/2) * (W/nf + 0.29)' nrd='0.29 / W' nrs='0.29 / W'
+ sa=0 sb=0 sd=0 mult=1 m=1
XM152 GND GND net22 GND sky130_fd_pr__nfet_01v8 L={L} W={W/2} nf=1 ad='int((nf+1)/2) * W/nf * 0.29' as='int((nf+2)/2) * W/nf * 0.29'
+ pd='2*int((nf+1)/2) * (W/nf + 0.29)' ps='2*int((nf+2)/2) * (W/nf + 0.29)' nrd='0.29 / W' nrs='0.29 / W'
+ sa=0 sb=0 sd=0 mult=1 m=1
X1 GND Vbn b0out b0 mux
X2 GND Vbn b1out b1 mux
X3 GND Vbn net43 b2 mux
X4 GND Vbn net45 b3 mux
X5 GND Vbn net44 b4 mux
X6 GND Vbn net42 b5 mux
X8 GND Vbn b6out b6 mux
Vout1 net10 net40 0
.save i(vout1)
XM38 net34 net21 net33 GND sky130_fd_pr__nfet_01v8 L={L} W={W} nf=1 ad='int((nf+1)/2) * W/nf * 0.29'
+ as='int((nf+2)/2) * W/nf * 0.29' pd='2*int((nf+1)/2) * (W/nf + 0.29)' ps='2*int((nf+2)/2) * (W/nf + 0.29)'
+ nrd='0.29 / W' nrs='0.29 / W' sa=0 sb=0 sd=0 mult=1 m=1
XM39 net33 net21 net34 GND sky130_fd_pr__nfet_01v8 L={L} W={W} nf=1 ad='int((nf+1)/2) * W/nf * 0.29'
+ as='int((nf+2)/2) * W/nf * 0.29' pd='2*int((nf+1)/2) * (W/nf + 0.29)' ps='2*int((nf+2)/2) * (W/nf + 0.29)'
+ nrd='0.29 / W' nrs='0.29 / W' sa=0 sb=0 sd=0 mult=1 m=1
XM40 net34 net21 net35 GND sky130_fd_pr__nfet_01v8 L={L} W={W} nf=1 ad='int((nf+1)/2) * W/nf * 0.29'
+ as='int((nf+2)/2) * W/nf * 0.29' pd='2*int((nf+1)/2) * (W/nf + 0.29)' ps='2*int((nf+2)/2) * (W/nf + 0.29)'
+ nrd='0.29 / W' nrs='0.29 / W' sa=0 sb=0 sd=0 mult=1 m=1
XM41 net35 net21 net34 GND sky130_fd_pr__nfet_01v8 L={L} W={W} nf=1 ad='int((nf+1)/2) * W/nf * 0.29'
+ as='int((nf+2)/2) * W/nf * 0.29' pd='2*int((nf+1)/2) * (W/nf + 0.29)' ps='2*int((nf+2)/2) * (W/nf + 0.29)'
+ nrd='0.29 / W' nrs='0.29 / W' sa=0 sb=0 sd=0 mult=1 m=1
XM42 GND b0out net34 GND sky130_fd_pr__nfet_01v8 L={L} W={W} nf=1 ad='int((nf+1)/2) * W/nf * 0.29' as='int((nf+2)/2) * W/nf * 0.29'
+ pd='2*int((nf+1)/2) * (W/nf + 0.29)' ps='2*int((nf+2)/2) * (W/nf + 0.29)' nrd='0.29 / W' nrs='0.29 / W'
+ sa=0 sb=0 sd=0 mult=1 m=1
XM43 net33 b1out GND GND sky130_fd_pr__nfet_01v8 L={L} W={W} nf=1 ad='int((nf+1)/2) * W/nf * 0.29' as='int((nf+2)/2) * W/nf * 0.29'
+ pd='2*int((nf+1)/2) * (W/nf + 0.29)' ps='2*int((nf+2)/2) * (W/nf + 0.29)' nrd='0.29 / W' nrs='0.29 / W'
+ sa=0 sb=0 sd=0 mult=1 m=1
XM44 GND net42 net36 GND sky130_fd_pr__nfet_01v8 L={L} W={W} nf=1 ad='int((nf+1)/2) * W/nf * 0.29' as='int((nf+2)/2) * W/nf * 0.29'
+ pd='2*int((nf+1)/2) * (W/nf + 0.29)' ps='2*int((nf+2)/2) * (W/nf + 0.29)' nrd='0.29 / W' nrs='0.29 / W'
+ sa=0 sb=0 sd=0 mult=1 m=1
XM45 net33 net21 net37 GND sky130_fd_pr__nfet_01v8 L={L} W={W} nf=1 ad='int((nf+1)/2) * W/nf * 0.29'
+ as='int((nf+2)/2) * W/nf * 0.29' pd='2*int((nf+1)/2) * (W/nf + 0.29)' ps='2*int((nf+2)/2) * (W/nf + 0.29)'
+ nrd='0.29 / W' nrs='0.29 / W' sa=0 sb=0 sd=0 mult=1 m=1
XM46 net37 net21 net33 GND sky130_fd_pr__nfet_01v8 L={L} W={W} nf=1 ad='int((nf+1)/2) * W/nf * 0.29'
+ as='int((nf+2)/2) * W/nf * 0.29' pd='2*int((nf+1)/2) * (W/nf + 0.29)' ps='2*int((nf+2)/2) * (W/nf + 0.29)'
+ nrd='0.29 / W' nrs='0.29 / W' sa=0 sb=0 sd=0 mult=1 m=1
XM96 net33 net21 net35 GND sky130_fd_pr__nfet_01v8 L={L} W={W} nf=1 ad='int((nf+1)/2) * W/nf * 0.29'
+ as='int((nf+2)/2) * W/nf * 0.29' pd='2*int((nf+1)/2) * (W/nf + 0.29)' ps='2*int((nf+2)/2) * (W/nf + 0.29)'
+ nrd='0.29 / W' nrs='0.29 / W' sa=0 sb=0 sd=0 mult=1 m=1
XM97 net35 net21 net37 GND sky130_fd_pr__nfet_01v8 L={L} W={W} nf=1 ad='int((nf+1)/2) * W/nf * 0.29'
+ as='int((nf+2)/2) * W/nf * 0.29' pd='2*int((nf+1)/2) * (W/nf + 0.29)' ps='2*int((nf+2)/2) * (W/nf + 0.29)'
+ nrd='0.29 / W' nrs='0.29 / W' sa=0 sb=0 sd=0 mult=1 m=1
XM98 net37 net21 net38 GND sky130_fd_pr__nfet_01v8 L={L} W={W} nf=1 ad='int((nf+1)/2) * W/nf * 0.29'
+ as='int((nf+2)/2) * W/nf * 0.29' pd='2*int((nf+1)/2) * (W/nf + 0.29)' ps='2*int((nf+2)/2) * (W/nf + 0.29)'
+ nrd='0.29 / W' nrs='0.29 / W' sa=0 sb=0 sd=0 mult=1 m=1
XM99 net38 net21 net37 GND sky130_fd_pr__nfet_01v8 L={L} W={W} nf=1 ad='int((nf+1)/2) * W/nf * 0.29'
+ as='int((nf+2)/2) * W/nf * 0.29' pd='2*int((nf+1)/2) * (W/nf + 0.29)' ps='2*int((nf+2)/2) * (W/nf + 0.29)'
+ nrd='0.29 / W' nrs='0.29 / W' sa=0 sb=0 sd=0 mult=1 m=1
XM100 GND net43 net37 GND sky130_fd_pr__nfet_01v8 L={L} W={W} nf=1 ad='int((nf+1)/2) * W/nf * 0.29' as='int((nf+2)/2) * W/nf * 0.29'
+ pd='2*int((nf+1)/2) * (W/nf + 0.29)' ps='2*int((nf+2)/2) * (W/nf + 0.29)' nrd='0.29 / W' nrs='0.29 / W'
+ sa=0 sb=0 sd=0 mult=1 m=1
XM101 net39 net21 net36 GND sky130_fd_pr__nfet_01v8 L={L} W={W} nf=1 ad='int((nf+1)/2) * W/nf * 0.29'
+ as='int((nf+2)/2) * W/nf * 0.29' pd='2*int((nf+1)/2) * (W/nf + 0.29)' ps='2*int((nf+2)/2) * (W/nf + 0.29)'
+ nrd='0.29 / W' nrs='0.29 / W' sa=0 sb=0 sd=0 mult=1 m=1
XM102 net36 net21 net39 GND sky130_fd_pr__nfet_01v8 L={L} W={W} nf=1 ad='int((nf+1)/2) * W/nf * 0.29'
+ as='int((nf+2)/2) * W/nf * 0.29' pd='2*int((nf+1)/2) * (W/nf + 0.29)' ps='2*int((nf+2)/2) * (W/nf + 0.29)'
+ nrd='0.29 / W' nrs='0.29 / W' sa=0 sb=0 sd=0 mult=1 m=1
XM103 net35 net21 net36 GND sky130_fd_pr__nfet_01v8 L={L} W={W} nf=1 ad='int((nf+1)/2) * W/nf * 0.29'
+ as='int((nf+2)/2) * W/nf * 0.29' pd='2*int((nf+1)/2) * (W/nf + 0.29)' ps='2*int((nf+2)/2) * (W/nf + 0.29)'
+ nrd='0.29 / W' nrs='0.29 / W' sa=0 sb=0 sd=0 mult=1 m=1
XM104 net39 net21 net35 GND sky130_fd_pr__nfet_01v8 L={L} W={W} nf=1 ad='int((nf+1)/2) * W/nf * 0.29'
+ as='int((nf+2)/2) * W/nf * 0.29' pd='2*int((nf+1)/2) * (W/nf + 0.29)' ps='2*int((nf+2)/2) * (W/nf + 0.29)'
+ nrd='0.29 / W' nrs='0.29 / W' sa=0 sb=0 sd=0 mult=1 m=1
XM105 net38 net21 net39 GND sky130_fd_pr__nfet_01v8 L={L} W={W} nf=1 ad='int((nf+1)/2) * W/nf * 0.29'
+ as='int((nf+2)/2) * W/nf * 0.29' pd='2*int((nf+1)/2) * (W/nf + 0.29)' ps='2*int((nf+2)/2) * (W/nf + 0.29)'
+ nrd='0.29 / W' nrs='0.29 / W' sa=0 sb=0 sd=0 mult=1 m=1
XM106 net39 net21 net38 GND sky130_fd_pr__nfet_01v8 L={L} W={W} nf=1 ad='int((nf+1)/2) * W/nf * 0.29'
+ as='int((nf+2)/2) * W/nf * 0.29' pd='2*int((nf+1)/2) * (W/nf + 0.29)' ps='2*int((nf+2)/2) * (W/nf + 0.29)'
+ nrd='0.29 / W' nrs='0.29 / W' sa=0 sb=0 sd=0 mult=1 m=1
XM107 net39 net44 GND GND sky130_fd_pr__nfet_01v8 L={L} W={W} nf=1 ad='int((nf+1)/2) * W/nf * 0.29' as='int((nf+2)/2) * W/nf * 0.29'
+ pd='2*int((nf+1)/2) * (W/nf + 0.29)' ps='2*int((nf+2)/2) * (W/nf + 0.29)' nrd='0.29 / W' nrs='0.29 / W'
+ sa=0 sb=0 sd=0 mult=1 m=1
XM108 net40 net21 net41 GND sky130_fd_pr__nfet_01v8 L={L} W={W} nf=1 ad='int((nf+1)/2) * W/nf * 0.29'
+ as='int((nf+2)/2) * W/nf * 0.29' pd='2*int((nf+1)/2) * (W/nf + 0.29)' ps='2*int((nf+2)/2) * (W/nf + 0.29)'
+ nrd='0.29 / W' nrs='0.29 / W' sa=0 sb=0 sd=0 mult=1 m=1
XM109 net41 net21 net40 GND sky130_fd_pr__nfet_01v8 L={L} W={W} nf=1 ad='int((nf+1)/2) * W/nf * 0.29'
+ as='int((nf+2)/2) * W/nf * 0.29' pd='2*int((nf+1)/2) * (W/nf + 0.29)' ps='2*int((nf+2)/2) * (W/nf + 0.29)'
+ nrd='0.29 / W' nrs='0.29 / W' sa=0 sb=0 sd=0 mult=1 m=1
XM110 net36 net21 net41 GND sky130_fd_pr__nfet_01v8 L={L} W={W} nf=1 ad='int((nf+1)/2) * W/nf * 0.29'
+ as='int((nf+2)/2) * W/nf * 0.29' pd='2*int((nf+1)/2) * (W/nf + 0.29)' ps='2*int((nf+2)/2) * (W/nf + 0.29)'
+ nrd='0.29 / W' nrs='0.29 / W' sa=0 sb=0 sd=0 mult=1 m=1
XM111 net41 net21 net36 GND sky130_fd_pr__nfet_01v8 L={L} W={W} nf=1 ad='int((nf+1)/2) * W/nf * 0.29'
+ as='int((nf+2)/2) * W/nf * 0.29' pd='2*int((nf+1)/2) * (W/nf + 0.29)' ps='2*int((nf+2)/2) * (W/nf + 0.29)'
+ nrd='0.29 / W' nrs='0.29 / W' sa=0 sb=0 sd=0 mult=1 m=1
XM112 net41 b6out GND GND sky130_fd_pr__nfet_01v8 L={L} W={W} nf=1 ad='int((nf+1)/2) * W/nf * 0.29' as='int((nf+2)/2) * W/nf * 0.29'
+ pd='2*int((nf+1)/2) * (W/nf + 0.29)' ps='2*int((nf+2)/2) * (W/nf + 0.29)' nrd='0.29 / W' nrs='0.29 / W'
+ sa=0 sb=0 sd=0 mult=1 m=1
XM113 GND net45 net38 GND sky130_fd_pr__nfet_01v8 L={L} W={W} nf=1 ad='int((nf+1)/2) * W/nf * 0.29' as='int((nf+2)/2) * W/nf * 0.29'
+ pd='2*int((nf+1)/2) * (W/nf + 0.29)' ps='2*int((nf+2)/2) * (W/nf + 0.29)' nrd='0.29 / W' nrs='0.29 / W'
+ sa=0 sb=0 sd=0 mult=1 m=1
XM114 net35 net21 net38 GND sky130_fd_pr__nfet_01v8 L={L} W={W} nf=1 ad='int((nf+1)/2) * W/nf * 0.29'
+ as='int((nf+2)/2) * W/nf * 0.29' pd='2*int((nf+1)/2) * (W/nf + 0.29)' ps='2*int((nf+2)/2) * (W/nf + 0.29)'
+ nrd='0.29 / W' nrs='0.29 / W' sa=0 sb=0 sd=0 mult=1 m=1
XM115 VDD net35 net35 VDD sky130_fd_pr__pfet_01v8 L={L} W={W} nf=1 ad='int((nf+1)/2) * W/nf * 0.29' as='int((nf+2)/2) * W/nf * 0.29'
+ pd='2*int((nf+1)/2) * (W/nf + 0.29)' ps='2*int((nf+2)/2) * (W/nf + 0.29)' nrd='0.29 / W' nrs='0.29 / W'
+ sa=0 sb=0 sd=0 mult=1 m=1
**** begin user architecture code

.param W=24
.param L=1
.control
set wr_vecnames
set wr_singlescale
let code = 0
  while code < 128
    if code eq 0
      let b0 = 0
    else
      let b0 = code % 2 * 1.8
    end
    if floor(code / 2) eq 0
      let b1 = 0
    else
      let b1 = floor(code / 2) % 2 * 1.8
    end
    if floor(code / 4) eq 0
      let b2 = 0
    else
      let b2 = floor(code / 4) % 2 * 1.8
    end
    if floor(code / 8) eq 0
      let b3 = 0
    else
      let b3 = floor(code / 8) % 2 * 1.8
    end
    if floor(code / 16) eq 0
      let b4 = 0
    else
      let b4 = floor(code / 16) % 2 * 1.8
    end
    if floor(code / 32) eq 0
      let b5 = 0
    else
      let b5 = floor(code / 32) % 2 * 1.8
    end
    if floor(code / 64) eq 0
      let b6 = 0
    else
      let b6 = floor(code / 64) % 2 * 1.8
    end
    alter v0 $&b0
    alter v1 $&b1
    alter v2 $&b2
    alter v3 $&b3
    alter v4 $&b4
    alter v5 $&b5
    alter v6 $&b6
    save all
    op
    wrdata ~/Documents/current-output-dac-vlsi/simulations/dac_sim.txt v(Vbn) i(Vout) i(Vout1) v(b6)
+ v(b5) v(b4) v(b3) v(b2) v(b1) v(b0) v(b0out) v(b1out) v(b6out)
    if code eq 0
      set appendwrite
      set wr_vecnames = FALSE
    end
    let code = code + 1
  end
.endc


.option wnflag=1
.param MC_SWITCH=0.0
.lib ~/skywater/skywater-pdk/libraries/sky130_fd_pr_ngspice/latest/models/sky130.lib.spice tt

**** end user architecture code
**.ends

* expanding   symbol:  /home/madvlsi/Documents/current-output-dac-vlsi/schematics/mux.sym # of
*+ pins=4
** sym_path: dac/schematics/mux.sym
** sch_path: dac/schematics/mux.sch
.subckt mux A B Y S
*.ipin A
*.ipin B
*.ipin S
*.opin Y
XM1 A S Y VDD sky130_fd_pr__pfet_01v8 L=0.15 W=1 nf=1 ad='int((nf+1)/2) * W/nf * 0.29' as='int((nf+2)/2) * W/nf * 0.29'
+ pd='2*int((nf+1)/2) * (W/nf + 0.29)' ps='2*int((nf+2)/2) * (W/nf + 0.29)' nrd='0.29 / W' nrs='0.29 / W'
+ sa=0 sb=0 sd=0 mult=1 m=1
XM3 net1 S VDD VDD sky130_fd_pr__pfet_01v8 L=0.15 W=1 nf=1 ad='int((nf+1)/2) * W/nf * 0.29' as='int((nf+2)/2) * W/nf * 0.29'
+ pd='2*int((nf+1)/2) * (W/nf + 0.29)' ps='2*int((nf+2)/2) * (W/nf + 0.29)' nrd='0.29 / W' nrs='0.29 / W'
+ sa=0 sb=0 sd=0 mult=1 m=1
XM4 net1 S GND GND sky130_fd_pr__nfet_01v8 L=0.15 W=1 nf=1 ad='int((nf+1)/2) * W/nf * 0.29' as='int((nf+2)/2) * W/nf * 0.29'
+ pd='2*int((nf+1)/2) * (W/nf + 0.29)' ps='2*int((nf+2)/2) * (W/nf + 0.29)' nrd='0.29 / W' nrs='0.29 / W'
+ sa=0 sb=0 sd=0 mult=1 m=1
XM5 A net1 Y GND sky130_fd_pr__nfet_01v8 L=0.15 W=1 nf=1 ad='int((nf+1)/2) * W/nf * 0.29' as='int((nf+2)/2) * W/nf * 0.29'
+ pd='2*int((nf+1)/2) * (W/nf + 0.29)' ps='2*int((nf+2)/2) * (W/nf + 0.29)' nrd='0.29 / W' nrs='0.29 / W'
+ sa=0 sb=0 sd=0 mult=1 m=1
XM2 B net1 Y VDD sky130_fd_pr__pfet_01v8 L=0.15 W=1 nf=1 ad='int((nf+1)/2) * W/nf * 0.29' as='int((nf+2)/2) * W/nf * 0.29'
+ pd='2*int((nf+1)/2) * (W/nf + 0.29)' ps='2*int((nf+2)/2) * (W/nf + 0.29)' nrd='0.29 / W' nrs='0.29 / W'
+ sa=0 sb=0 sd=0 mult=1 m=1
XM6 B S Y GND sky130_fd_pr__nfet_01v8 L=0.15 W=1 nf=1 ad='int((nf+1)/2) * W/nf * 0.29' as='int((nf+2)/2) * W/nf * 0.29'
+ pd='2*int((nf+1)/2) * (W/nf + 0.29)' ps='2*int((nf+2)/2) * (W/nf + 0.29)' nrd='0.29 / W' nrs='0.29 / W'
+ sa=0 sb=0 sd=0 mult=1 m=1
.ends

.GLOBAL GND
.GLOBAL VDD
.end
